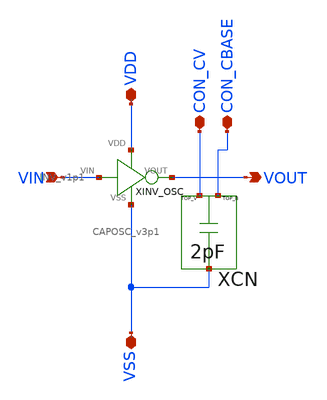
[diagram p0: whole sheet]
** sch_path: modules/INVandCAP_v4p1/symbol/INVandCAP_v4p1.sch
**.subckt INVandCAP_v4p1 VIN VDD VSS VOUT CON_CV CON_CBASE
*.ipin VIN
*.iopin VDD
*.iopin VSS
*.opin VOUT
*.iopin CON_CV
*.iopin CON_CBASE
XINV_OSC VIN VOUT VDD VSS INV_v1p1
XCN CON_CV CON_CBASE VSS CAPOSC_v3p1
**.ends
.end
